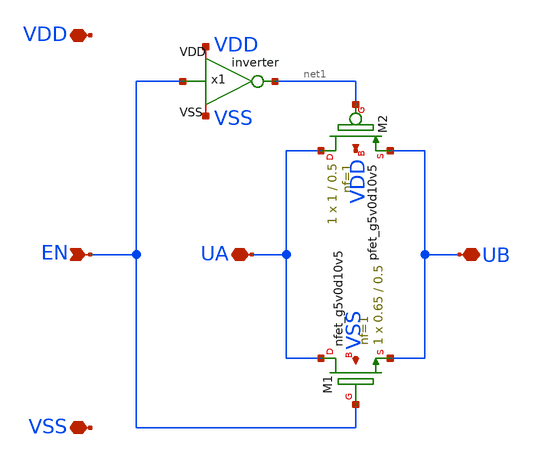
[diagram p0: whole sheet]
** sch_path: xschem/passgate.sch
**.subckt passgate VSS VDD UA UB EN
*.iopin VSS
*.iopin VDD
*.iopin UA
*.iopin UB
*.ipin EN
XM1 UA EN UB VSS sky130_fd_pr__nfet_g5v0d10v5 L=0.5 W=0.65 nf=1 ad='int((1 + 1)/2) * 0.65 / 1 * 0.29'
+ as='int((1 + 2)/2) * 0.65 / 1 * 0.29' pd='2*int((1 + 1)/2) * (0.65 / 1 + 0.29)' ps='2*int((1 + 2)/2) * (0.65 / 1 + 0.29)'
+ nrd='0.29 / 0.65 ' nrs='0.29 / 0.65 ' sa=0 sb=0 sd=0 mult=1 m=1
XM2 UA net1 UB VDD sky130_fd_pr__pfet_g5v0d10v5 L=0.5 W=1 nf=1 ad='int((1 + 1)/2) * 1 / 1 * 0.29' as='int((1 + 2)/2) * 1 / 1 * 0.29'
+ pd='2*int((1 + 1)/2) * (1 / 1 + 0.29)' ps='2*int((1 + 2)/2) * (1 / 1 + 0.29)' nrd='0.29 / 1 ' nrs='0.29 / 1 '
+ sa=0 sb=0 sd=0 mult=1 m=1
x1 VDD EN net1 VSS inverter
**.ends

* expanding   symbol:  inverter.sym # of pins=4
** sym_path: xschem/inverter.sym
** sch_path: xschem/inverter.sch
.subckt inverter VDD IN OUT VSS
*.iopin VSS
*.iopin VDD
*.ipin IN
*.opin OUT
XM1 OUT IN VSS VSS sky130_fd_pr__nfet_g5v0d10v5 L=0.5 W=0.65 nf=1 ad='int((1 + 1)/2) * 0.65 / 1 * 0.29'
+ as='int((1 + 2)/2) * 0.65 / 1 * 0.29' pd='2*int((1 + 1)/2) * (0.65 / 1 + 0.29)' ps='2*int((1 + 2)/2) * (0.65 / 1 + 0.29)'
+ nrd='0.29 / 0.65 ' nrs='0.29 / 0.65 ' sa=0 sb=0 sd=0 mult=1 m=1
XM2 OUT IN VDD VDD sky130_fd_pr__pfet_g5v0d10v5 L=0.5 W=1 nf=1 ad='int((1 + 1)/2) * 1 / 1 * 0.29' as='int((1 + 2)/2) * 1 / 1 * 0.29'
+ pd='2*int((1 + 1)/2) * (1 / 1 + 0.29)' ps='2*int((1 + 2)/2) * (1 / 1 + 0.29)' nrd='0.29 / 1 ' nrs='0.29 / 1 '
+ sa=0 sb=0 sd=0 mult=1 m=1
.ends

.end
